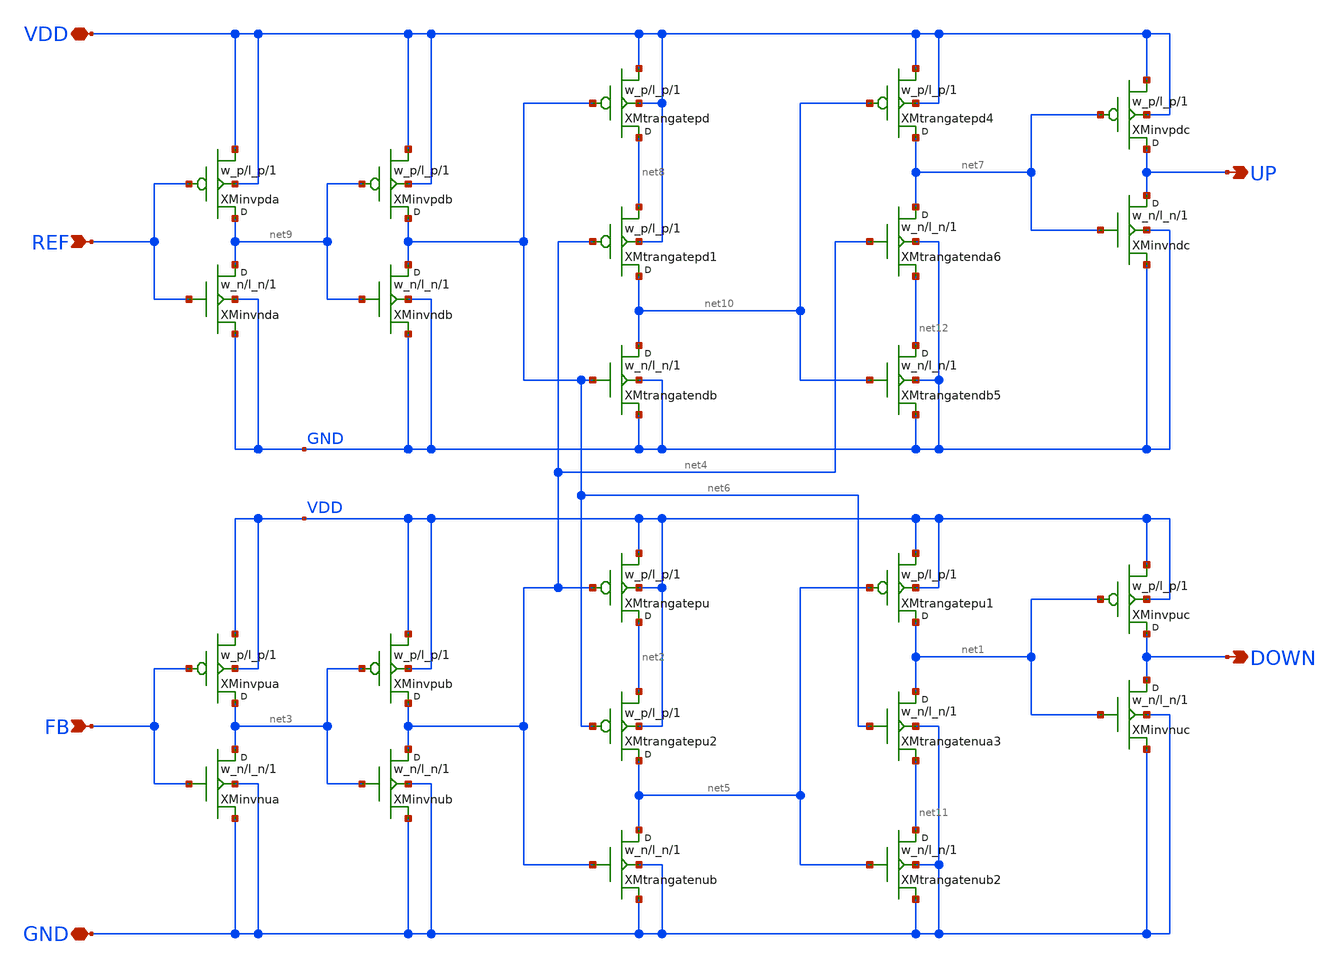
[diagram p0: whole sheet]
** sch_path: design/phasefrequencydetector_ff/phasefrequencydetector_ff.sch
**.subckt phasefrequencydetector_ff FB DOWN VDD GND UP REF
*.ipin FB
*.opin DOWN
*.iopin VDD
*.iopin GND
*.opin UP
*.ipin REF
XMtrangatepu net2 net4 VDD VDD pe w=w_p l=l_p m=1
XMtrangatenub net5 net4 GND GND ne w=w_n l=l_n m=1
XMinvpuc DOWN net1 VDD VDD pe w=w_p l=l_p m=1
XMinvnuc DOWN net1 GND GND ne w=w_n l=l_n m=1
XMinvpub net4 net3 VDD VDD pe w=w_p l=l_p m=1
XMinvnub net4 net3 GND GND ne w=w_n l=l_n m=1
XMinvpua net3 FB VDD VDD pe w=w_p l=l_p m=1
XMinvnua net3 FB GND GND ne w=w_n l=l_n m=1
XMtrangatepd net8 net6 VDD VDD pe w=w_p l=l_p m=1
XMtrangatendb net10 net6 GND GND ne w=w_n l=l_n m=1
XMinvpdc UP net7 VDD VDD pe w=w_p l=l_p m=1
XMinvndc UP net7 GND GND ne w=w_n l=l_n m=1
XMinvpdb net6 net9 VDD VDD pe w=w_p l=l_p m=1
XMinvndb net6 net9 GND GND ne w=w_n l=l_n m=1
XMinvpda net9 REF VDD VDD pe w=w_p l=l_p m=1
XMinvnda net9 REF GND GND ne w=w_n l=l_n m=1
XMtrangatepu1 net1 net5 VDD VDD pe w=w_p l=l_p m=1
XMtrangatenub2 net11 net5 GND GND ne w=w_n l=l_n m=1
XMtrangatenua3 net1 net6 net11 GND ne w=w_n l=l_n m=1
XMtrangatepd4 net7 net10 VDD VDD pe w=w_p l=l_p m=1
XMtrangatendb5 net12 net10 GND GND ne w=w_n l=l_n m=1
XMtrangatenda6 net7 net4 net12 GND ne w=w_n l=l_n m=1
XMtrangatepd1 net10 net4 net8 VDD pe w=w_p l=l_p m=1
XMtrangatepu2 net5 net6 net2 VDD pe w=w_p l=l_p m=1
**.ends
.end
